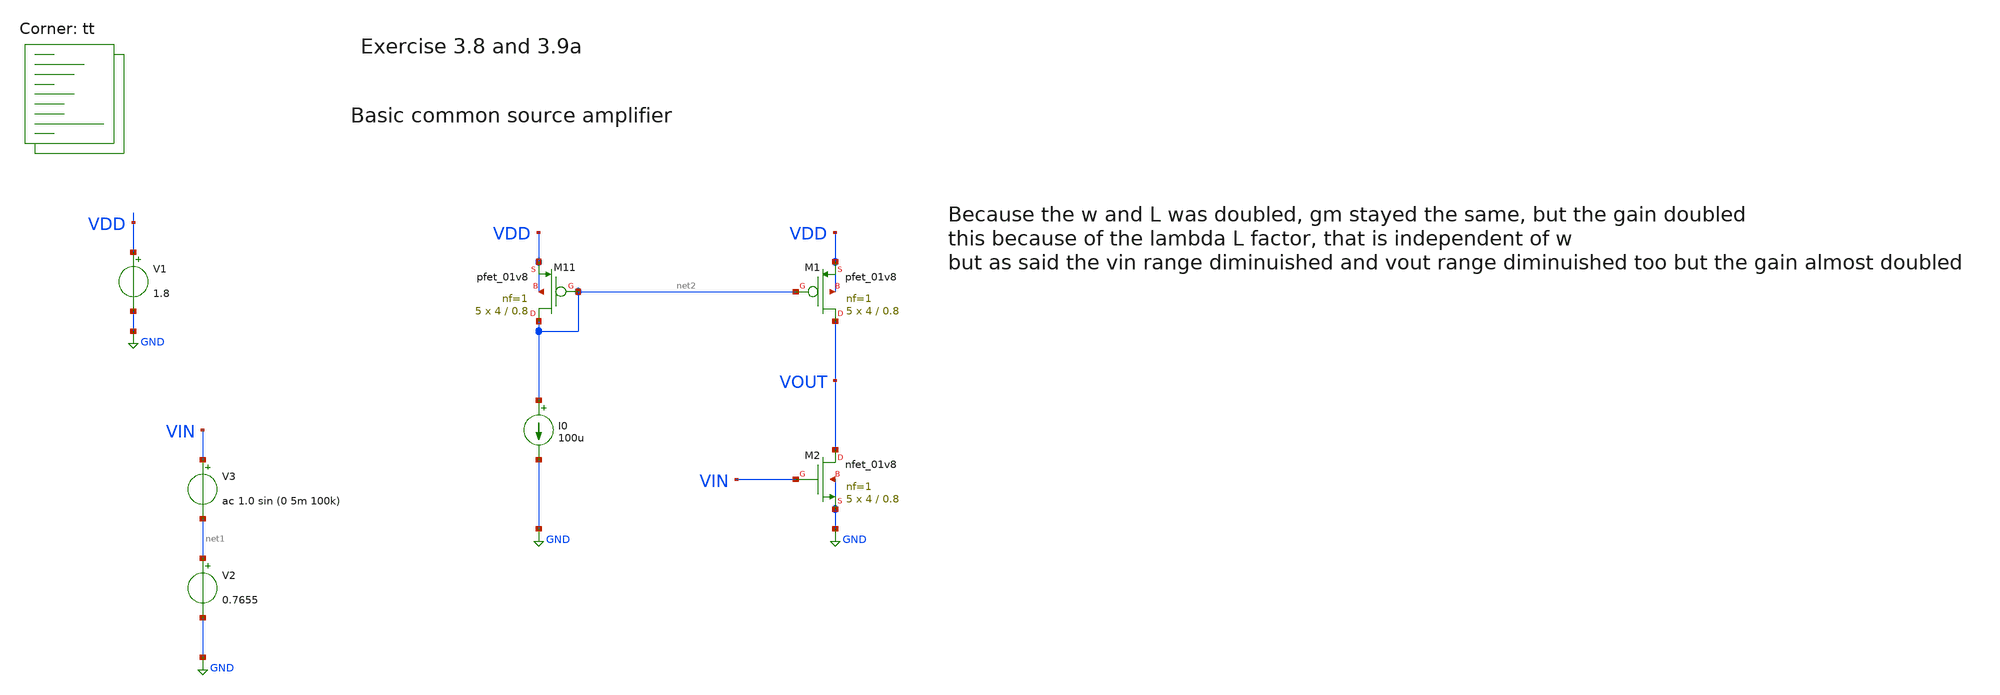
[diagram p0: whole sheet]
** sch_path: Analog_integrated_circuit_Design/chapter3/9/9.sch
**.subckt 9
V1 VDD GND 1.8
V2 net1 GND 0.7655
XM11 net2 net2 VDD VDD sky130_fd_pr__pfet_01v8 L=0.8 W=4 nf=1 ad='int((nf+1)/2) * W/nf * 0.29' as='int((nf+2)/2) * W/nf * 0.29'
+ pd='2*int((nf+1)/2) * (W/nf + 0.29)' ps='2*int((nf+2)/2) * (W/nf + 0.29)' nrd='0.29 / W' nrs='0.29 / W'
+ sa=0 sb=0 sd=0 mult=5 m=5
I0 net2 GND 100u
XM1 VOUT net2 VDD VDD sky130_fd_pr__pfet_01v8 L=0.8 W=4 nf=1 ad='int((nf+1)/2) * W/nf * 0.29' as='int((nf+2)/2) * W/nf * 0.29'
+ pd='2*int((nf+1)/2) * (W/nf + 0.29)' ps='2*int((nf+2)/2) * (W/nf + 0.29)' nrd='0.29 / W' nrs='0.29 / W'
+ sa=0 sb=0 sd=0 mult=5 m=5
XM2 VOUT VIN GND GND sky130_fd_pr__nfet_01v8 L=0.8 W=4 nf=1 ad='int((1 + 1)/2) * 4 / 1 * 0.29' as='int((1 + 2)/2) * 4 / 1 * 0.29'
+ pd='2*int((1 + 1)/2) * (4 / 1 + 0.29)' ps='2*int((1 + 2)/2) * (4 / 1 + 0.29)' nrd='0.29 / 4 ' nrs='0.29 / 4 '
+ sa=0 sb=0 sd=0 mult=5 m=5
V3 VIN net1 ac 1.0 sin (0 5m 100k)
**** begin user architecture code
.lib $::SKYWATER_MODELS/sky130.lib.spice tt

**************************************************************
**************************************************************
**************************************************************
**************************************************************
**************************************************************
*LIBs*********************************************************
**************************************************************
**************************************************************
**************************************************************
**************************************************************
**************************************************************
*.lib $::SKYWATER_MODELS/sky130.lib.spice tt
* chose the corners in the corner file
* tt_mm for mismatch
* ss ff sf fs standart corners
* ll hh lh hl capacitor and resistors corners
* mc for total process variation including corners
**************************************************************
**************************************************************
**************************************************************
**************************************************************
**************************************************************
*Corners/montecarlo options***********************************
**************************************************************
**************************************************************
**************************************************************
**************************************************************
**************************************************************
.TEMP 27
**************************************************************
**************************************************************
**************************************************************
**************************************************************
*SIMULATION and Plots*****************************************
**************************************************************
**************************************************************
**************************************************************
**************************************************************
.control
save all
dc V2 0 1.8 0.001
*dc simulation
plot deriv(V(Vout)) v(VOUT)

tran 10ns 20u
plot v(VOUT)
ac dec 20 1 50G
plot db(v(VOUT))

.endc

**** end user architecture code
**.ends
.GLOBAL GND
.end
